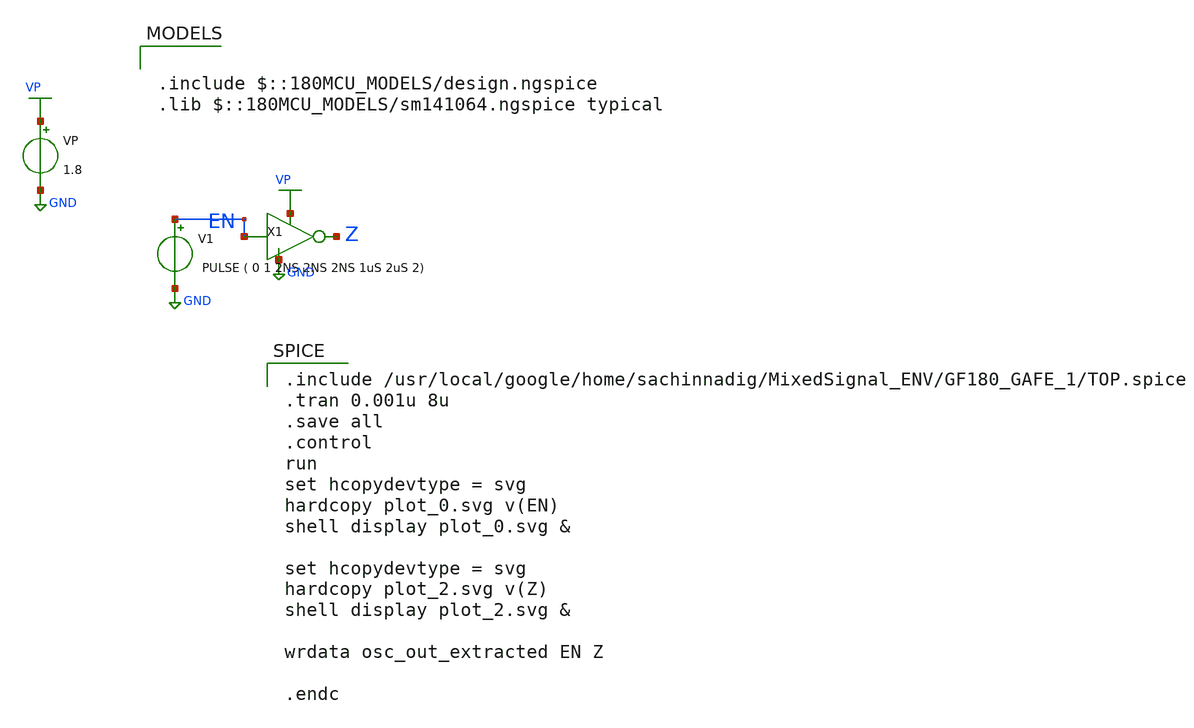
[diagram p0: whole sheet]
** sch_path: TOP_extracted.sch
**.subckt TOP_extracted
VP VP GND 1.8
V1 EN GND PULSE ( 0 1 2NS 2NS 2NS 1uS 2uS 2)
X1 VP Z GND EN TOP
**** begin user architecture code

.include $::180MCU_MODELS/design.ngspice
.lib $::180MCU_MODELS/sm141064.ngspice typical


.include /usr/local/google/home/sachinnadig/MixedSignal_ENV/GF180_GAFE_1/TOP.spice
.tran 0.001u 8u
.save all
.control
run
set hcopydevtype = svg
hardcopy plot_0.svg v(EN)
shell display plot_0.svg &

set hcopydevtype = svg
hardcopy plot_2.svg v(Z)
shell display plot_2.svg &

wrdata osc_out_extracted EN Z

.endc

**** end user architecture code
**.ends
.GLOBAL VP
.GLOBAL GND
.end
